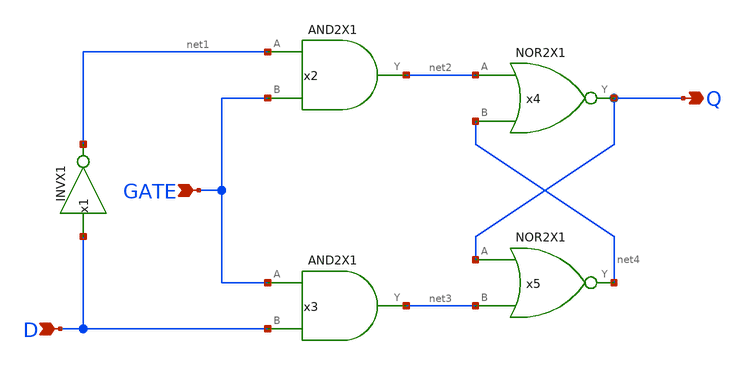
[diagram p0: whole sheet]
** sch_path: layout/xschem/sky130_rhbd/DLATCH.sch
**.subckt DLATCH Q D GATE
*.opin Q
*.ipin D
*.ipin GATE
x1 net1 D VDD VSS INVX1
x2 net2 net1 GATE VDD VSS AND2X1
x3 net3 GATE D VDD VSS AND2X1
x4 Q net2 net4 VDD VSS NOR2X1
x5 net4 Q net3 VDD VSS NOR2X1
**.ends
.end
